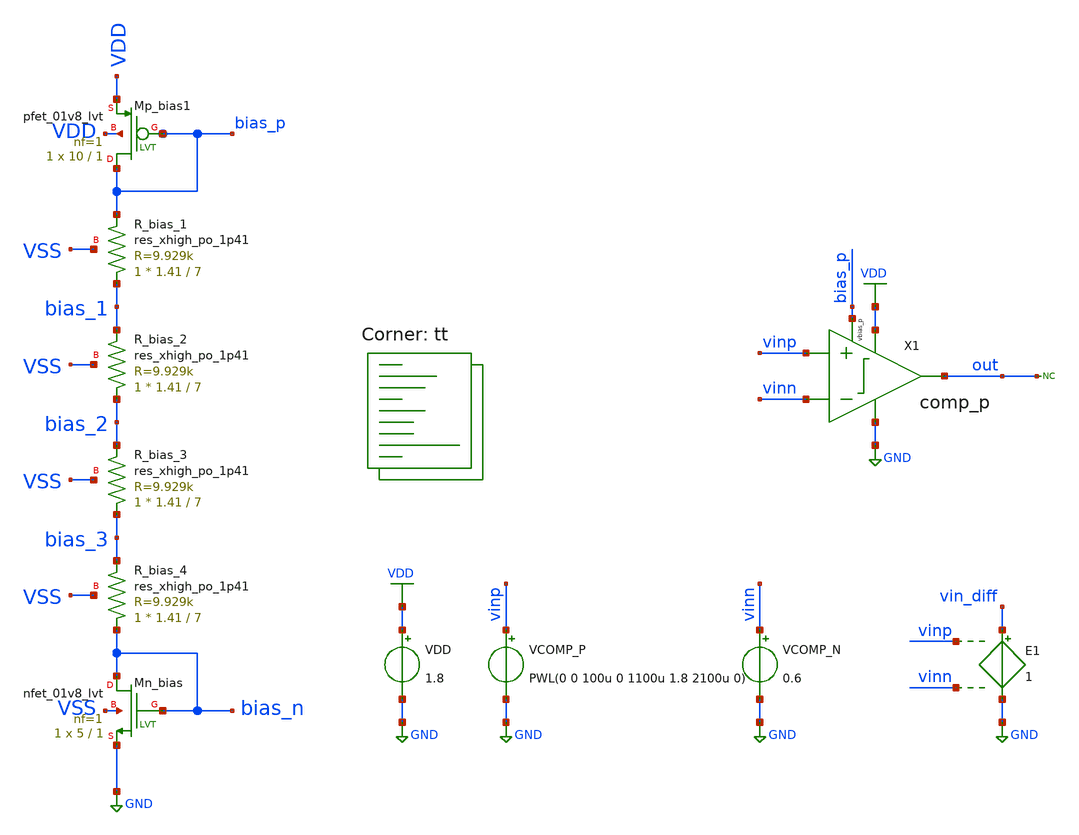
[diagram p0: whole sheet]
** sch_path: xsch/tb/comp_p/tb_comp_p_tran_sweep.sch
**.subckt tb_comp_p_tran_sweep
VDD VDD GND 1.8
* noconn out
VCOMP_N vinn GND 0.6
VCOMP_P vinp GND PWL(0 0 100u 0 1100u 1.8 2100u 0)
E1 vin_diff GND vinp vinn 1
XR_bias_1 bias_1 bias_p VSS sky130_fd_pr__res_xhigh_po_1p41 L=7 mult=1 m=1
XMn_bias bias_n bias_n GND VSS sky130_fd_pr__nfet_01v8_lvt L=1 W=5 nf=1 ad='int((nf+1)/2) * W/nf * 0.29'
+ as='int((nf+2)/2) * W/nf * 0.29' pd='2*int((nf+1)/2) * (W/nf + 0.29)' ps='2*int((nf+2)/2) * (W/nf + 0.29)'
+ nrd='0.29 / W' nrs='0.29 / W' sa=0 sb=0 sd=0 mult=1 m=1
XMp_bias1 bias_p bias_p VDD VDD sky130_fd_pr__pfet_01v8_lvt L=1 W=10 nf=1 ad='int((nf+1)/2) * W/nf * 0.29'
+ as='int((nf+2)/2) * W/nf * 0.29' pd='2*int((nf+1)/2) * (W/nf + 0.29)' ps='2*int((nf+2)/2) * (W/nf + 0.29)'
+ nrd='0.29 / W' nrs='0.29 / W' sa=0 sb=0 sd=0 mult=1 m=1
XR_bias_2 bias_2 bias_1 VSS sky130_fd_pr__res_xhigh_po_1p41 L=7 mult=1 m=1
XR_bias_3 bias_3 bias_2 VSS sky130_fd_pr__res_xhigh_po_1p41 L=7 mult=1 m=1
XR_bias_4 bias_n bias_3 VSS sky130_fd_pr__res_xhigh_po_1p41 L=7 mult=1 m=1
X1 vinp vinn bias_p out VDD GND comp_p
**** begin user architecture code



* control language script
.save X_COMP_P.latch_right
.save X_COMP_P.latch_left
.save vinp vinn out vdd
.save X_COMP_P.tail

.control
tran 0.1u 2100u

meas tran v_cross_lh FIND v(vinp) when v(out)=0.9 RISE=1
meas tran v_cross_hl FIND v(vinp) when v(out)=0.9 FALL=1

let v_th = v_cross_lh-0.6
let v_tl = v_cross_hl-0.6
let v_hyst = $&v_th - $&v_tl
let v_offset = $&v_th + $&v_tl

set xbrushwidth=2
plot v(out) v(vinp) v(vinn)
plot v(x_comp_p.latch_right) v(x_comp_p.latch_left)
plot v(X_COMP_P.tail)

echo V_th: $&v_th
echo V_tl: $&v_tl
echo V_hyst: $&v_hyst
echo V_offset: $&v_offset

rusage

.endc
.end



.lib $::SKYWATER_MODELS/sky130.lib.spice tt
**** end user architecture code
**.ends

* expanding   symbol:  /home/bmott/ttsky25b_tiny_chaos/xsch/ip/comparators/comp_p/comp_p.sym # of
*+ pins=6
** sym_path: /home/bmott/ttsky25b_tiny_chaos/xsch/ip/comparators/comp_p/comp_p.sym
** sch_path: /home/bmott/ttsky25b_tiny_chaos/xsch/ip/comparators/comp_p/comp_p.sch
.subckt comp_p vinp vinn vbias_p vout vdd vss
*.iopin vdd
*.iopin vss
*.ipin vbias_p
*.ipin vinn
*.ipin vinp
*.opin vout
XMp_inn1 latch_left vinn tail vdd sky130_fd_pr__pfet_01v8_lvt L=0.35 W=10 nf=1 ad='int((nf+1)/2) * W/nf * 0.29'
+ as='int((nf+2)/2) * W/nf * 0.29' pd='2*int((nf+1)/2) * (W/nf + 0.29)' ps='2*int((nf+2)/2) * (W/nf + 0.29)'
+ nrd='0.29 / W' nrs='0.29 / W' sa=0 sb=0 sd=0 mult=4 m=4
XMp_inp1 latch_right vinp tail vdd sky130_fd_pr__pfet_01v8_lvt L=0.35 W=10 nf=1 ad='int((nf+1)/2) * W/nf * 0.29'
+ as='int((nf+2)/2) * W/nf * 0.29' pd='2*int((nf+1)/2) * (W/nf + 0.29)' ps='2*int((nf+2)/2) * (W/nf + 0.29)'
+ nrd='0.29 / W' nrs='0.29 / W' sa=0 sb=0 sd=0 mult=4 m=4
XMn_diode_left1 latch_left latch_left vss vss sky130_fd_pr__nfet_01v8_lvt L=1 W=4 nf=1 ad='int((nf+1)/2) * W/nf * 0.29'
+ as='int((nf+2)/2) * W/nf * 0.29' pd='2*int((nf+1)/2) * (W/nf + 0.29)' ps='2*int((nf+2)/2) * (W/nf + 0.29)'
+ nrd='0.29 / W' nrs='0.29 / W' sa=0 sb=0 sd=0 mult=1 m=1
XMn_cs_left latch_right latch_left vss vss sky130_fd_pr__nfet_01v8_lvt L=1 W=5 nf=1 ad='int((nf+1)/2) * W/nf * 0.29'
+ as='int((nf+2)/2) * W/nf * 0.29' pd='2*int((nf+1)/2) * (W/nf + 0.29)' ps='2*int((nf+2)/2) * (W/nf + 0.29)'
+ nrd='0.29 / W' nrs='0.29 / W' sa=0 sb=0 sd=0 mult=1 m=1
XMn_diode_right latch_right latch_right vss vss sky130_fd_pr__nfet_01v8_lvt L=1 W=4 nf=1 ad='int((nf+1)/2) * W/nf * 0.29'
+ as='int((nf+2)/2) * W/nf * 0.29' pd='2*int((nf+1)/2) * (W/nf + 0.29)' ps='2*int((nf+2)/2) * (W/nf + 0.29)'
+ nrd='0.29 / W' nrs='0.29 / W' sa=0 sb=0 sd=0 mult=1 m=1
XMn_cs_right1 latch_left latch_right vss vss sky130_fd_pr__nfet_01v8_lvt L=1 W=5 nf=1 ad='int((nf+1)/2) * W/nf * 0.29'
+ as='int((nf+2)/2) * W/nf * 0.29' pd='2*int((nf+1)/2) * (W/nf + 0.29)' ps='2*int((nf+2)/2) * (W/nf + 0.29)'
+ nrd='0.29 / W' nrs='0.29 / W' sa=0 sb=0 sd=0 mult=1 m=1
XMp_tail tail vbias_p vdd vdd sky130_fd_pr__pfet_01v8_lvt L=1 W=10 nf=1 ad='int((nf+1)/2) * W/nf * 0.29'
+ as='int((nf+2)/2) * W/nf * 0.29' pd='2*int((nf+1)/2) * (W/nf + 0.29)' ps='2*int((nf+2)/2) * (W/nf + 0.29)'
+ nrd='0.29 / W' nrs='0.29 / W' sa=0 sb=0 sd=0 mult=1 m=1
XMn_out_right vout latch_right vss vss sky130_fd_pr__nfet_01v8_lvt L=1 W=5 nf=1 ad='int((nf+1)/2) * W/nf * 0.29'
+ as='int((nf+2)/2) * W/nf * 0.29' pd='2*int((nf+1)/2) * (W/nf + 0.29)' ps='2*int((nf+2)/2) * (W/nf + 0.29)'
+ nrd='0.29 / W' nrs='0.29 / W' sa=0 sb=0 sd=0 mult=1 m=1
XMn_out_left out_left latch_left vss vss sky130_fd_pr__nfet_01v8_lvt L=1 W=5 nf=1 ad='int((nf+1)/2) * W/nf * 0.29'
+ as='int((nf+2)/2) * W/nf * 0.29' pd='2*int((nf+1)/2) * (W/nf + 0.29)' ps='2*int((nf+2)/2) * (W/nf + 0.29)'
+ nrd='0.29 / W' nrs='0.29 / W' sa=0 sb=0 sd=0 mult=1 m=1
XMp_diode_left1 out_left out_left vdd vdd sky130_fd_pr__pfet_01v8_lvt L=1 W=8 nf=1 ad='int((nf+1)/2) * W/nf * 0.29'
+ as='int((nf+2)/2) * W/nf * 0.29' pd='2*int((nf+1)/2) * (W/nf + 0.29)' ps='2*int((nf+2)/2) * (W/nf + 0.29)'
+ nrd='0.29 / W' nrs='0.29 / W' sa=0 sb=0 sd=0 mult=1 m=1
XMp_out vout out_left vdd vdd sky130_fd_pr__pfet_01v8_lvt L=1 W=8 nf=1 ad='int((nf+1)/2) * W/nf * 0.29'
+ as='int((nf+2)/2) * W/nf * 0.29' pd='2*int((nf+1)/2) * (W/nf + 0.29)' ps='2*int((nf+2)/2) * (W/nf + 0.29)'
+ nrd='0.29 / W' nrs='0.29 / W' sa=0 sb=0 sd=0 mult=1 m=1
.ends

.GLOBAL VDD
.GLOBAL GND
.end
